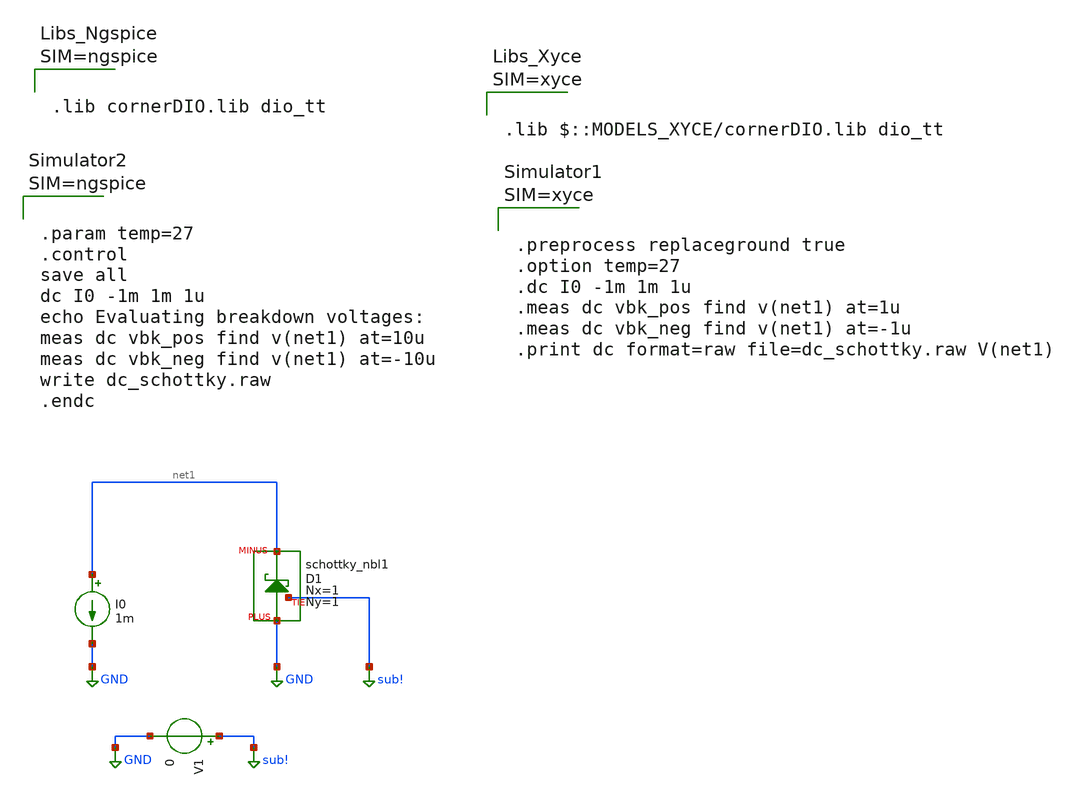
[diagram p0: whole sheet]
** sch_path: ihp-sg13g2/libs.tech/xschem/sg13g2_tests_xyce/dc_schottky.sch
* Copyright 2023 IHP PDK Authors
**.subckt dc_schottky
I0 net1 GND 1m
XD1 GND net1 sub! schottky_nbl1 Nx=1 Ny=1
V1 sub! GND 0
**** begin user architecture code









.lib cornerDIO.lib dio_tt






.param temp=27
.control
save all
dc I0 -1m 1m 1u
echo Evaluating breakdown voltages:
meas dc vbk_pos find v(net1) at=10u
meas dc vbk_neg find v(net1) at=-10u
write dc_schottky.raw
.endc



**** end user architecture code
**.ends
.GLOBAL GND
.GLOBAL sub!
.end
